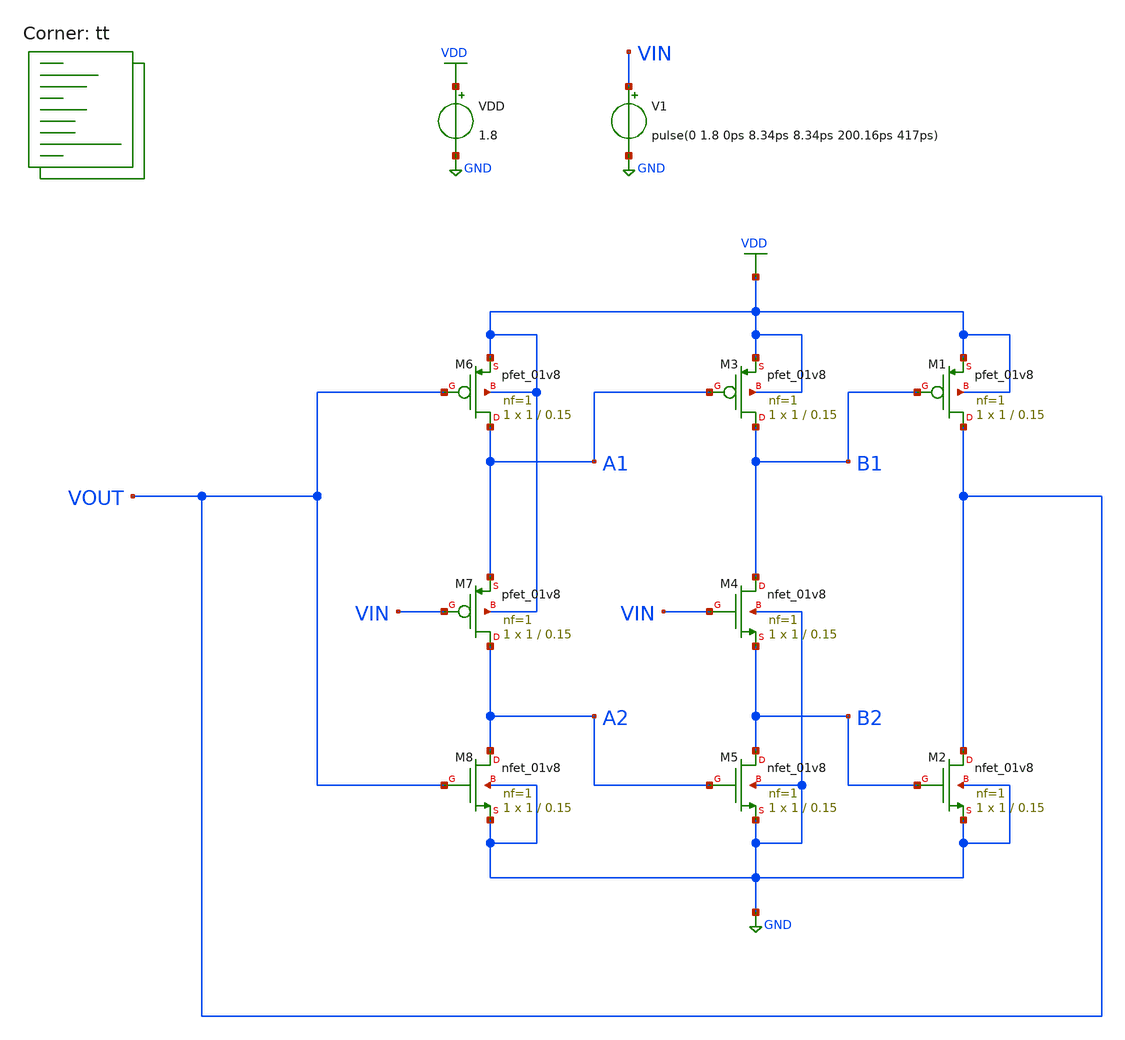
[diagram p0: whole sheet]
** sch_path: projects/pll/divider/xschem_ngspice/tb_TSPC_FF_split_path_3.sch
**.subckt tb_TSPC_FF_split_path_3
VDD VDD GND 1.8
V1 VIN GND pulse(0 1.8 0ps 8.34ps 8.34ps 200.16ps 417ps)
XM1 VOUT B1 VDD VDD sky130_fd_pr__pfet_01v8 L=0.15 W=1 nf=1 ad='int((nf+1)/2) * W/nf * 0.29' as='int((nf+2)/2) * W/nf * 0.29'
+ pd='2*int((nf+1)/2) * (W/nf + 0.29)' ps='2*int((nf+2)/2) * (W/nf + 0.29)' nrd='0.29 / W' nrs='0.29 / W'
+ sa=0 sb=0 sd=0 mult=1 m=1
XM4 B1 VIN B2 GND sky130_fd_pr__nfet_01v8 L=0.15 W=1 nf=1 ad='int((nf+1)/2) * W/nf * 0.29' as='int((nf+2)/2) * W/nf * 0.29'
+ pd='2*int((nf+1)/2) * (W/nf + 0.29)' ps='2*int((nf+2)/2) * (W/nf + 0.29)' nrd='0.29 / W' nrs='0.29 / W'
+ sa=0 sb=0 sd=0 mult=1 m=1
XM2 VOUT B2 GND GND sky130_fd_pr__nfet_01v8 L=0.15 W=1 nf=1 ad='int((nf+1)/2) * W/nf * 0.29' as='int((nf+2)/2) * W/nf * 0.29'
+ pd='2*int((nf+1)/2) * (W/nf + 0.29)' ps='2*int((nf+2)/2) * (W/nf + 0.29)' nrd='0.29 / W' nrs='0.29 / W'
+ sa=0 sb=0 sd=0 mult=1 m=1
XM3 B1 A1 VDD VDD sky130_fd_pr__pfet_01v8 L=0.15 W=1 nf=1 ad='int((nf+1)/2) * W/nf * 0.29' as='int((nf+2)/2) * W/nf * 0.29'
+ pd='2*int((nf+1)/2) * (W/nf + 0.29)' ps='2*int((nf+2)/2) * (W/nf + 0.29)' nrd='0.29 / W' nrs='0.29 / W'
+ sa=0 sb=0 sd=0 mult=1 m=1
XM5 B2 A2 GND GND sky130_fd_pr__nfet_01v8 L=0.15 W=1 nf=1 ad='int((nf+1)/2) * W/nf * 0.29' as='int((nf+2)/2) * W/nf * 0.29'
+ pd='2*int((nf+1)/2) * (W/nf + 0.29)' ps='2*int((nf+2)/2) * (W/nf + 0.29)' nrd='0.29 / W' nrs='0.29 / W'
+ sa=0 sb=0 sd=0 mult=1 m=1
XM6 A1 VOUT VDD VDD sky130_fd_pr__pfet_01v8 L=0.15 W=1 nf=1 ad='int((nf+1)/2) * W/nf * 0.29' as='int((nf+2)/2) * W/nf * 0.29'
+ pd='2*int((nf+1)/2) * (W/nf + 0.29)' ps='2*int((nf+2)/2) * (W/nf + 0.29)' nrd='0.29 / W' nrs='0.29 / W'
+ sa=0 sb=0 sd=0 mult=1 m=1
XM8 A2 VOUT GND GND sky130_fd_pr__nfet_01v8 L=0.15 W=1 nf=1 ad='int((nf+1)/2) * W/nf * 0.29' as='int((nf+2)/2) * W/nf * 0.29'
+ pd='2*int((nf+1)/2) * (W/nf + 0.29)' ps='2*int((nf+2)/2) * (W/nf + 0.29)' nrd='0.29 / W' nrs='0.29 / W'
+ sa=0 sb=0 sd=0 mult=1 m=1
XM7 A2 VIN A1 VDD sky130_fd_pr__pfet_01v8 L=0.15 W=1 nf=1 ad='int((nf+1)/2) * W/nf * 0.29' as='int((nf+2)/2) * W/nf * 0.29'
+ pd='2*int((nf+1)/2) * (W/nf + 0.29)' ps='2*int((nf+2)/2) * (W/nf + 0.29)' nrd='0.29 / W' nrs='0.29 / W'
+ sa=0 sb=0 sd=0 mult=1 m=1
**** begin user architecture code



.option method=gear
.option wnflag=1

.control

  save all
  tran 5p 20n
  remzerovec
  write tb_TSPC_FF_split_path_3.raw
  set appendwrite

.endc



.lib $::SKYWATER_MODELS/sky130.lib.spice tt
**** end user architecture code
**.ends
.GLOBAL GND
.GLOBAL VDD
.end
